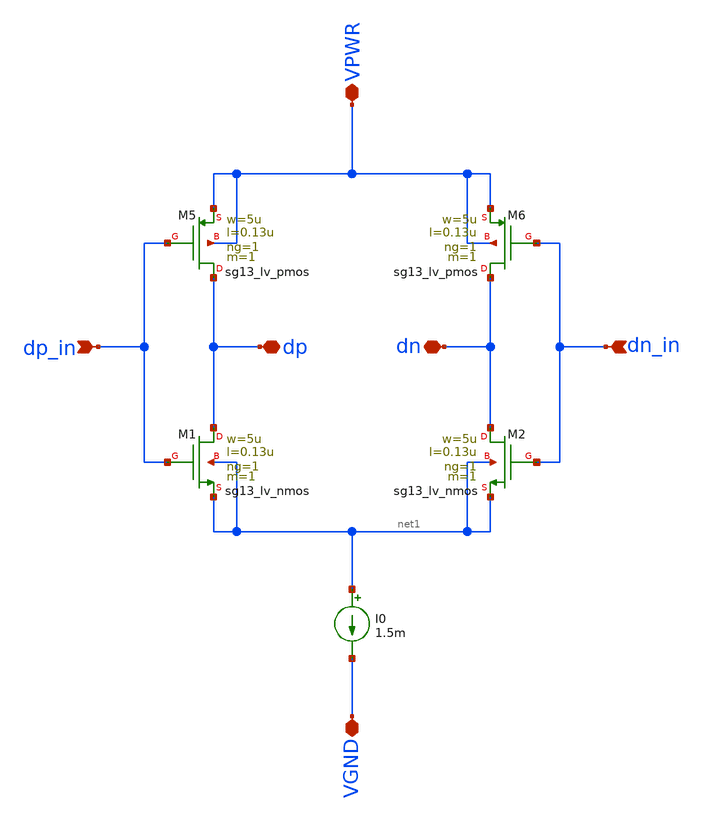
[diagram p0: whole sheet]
** sch_path: xschem/lvds_ideal.sch
**.subckt lvds_ideal dp_in dn_in VPWR VGND dp dn
*.ipin dp_in
*.ipin dn_in
*.iopin VPWR
*.iopin VGND
*.iopin dp
*.iopin dn
XM1 dp dp_in net1 net1 sg13_lv_nmos w=5u l=0.13u ng=1 m=1 mm_ok=1
XM2 dn dn_in net1 net1 sg13_lv_nmos w=5u l=0.13u ng=1 m=1 mm_ok=1
XM5 dp dp_in VPWR VPWR sg13_lv_pmos w=5u l=0.13u ng=1 m=1 mm_ok=1
XM6 dn dn_in VPWR VPWR sg13_lv_pmos w=5u l=0.13u ng=1 m=1 mm_ok=1
I0 net1 VGND 1.5m
**.ends
.end
